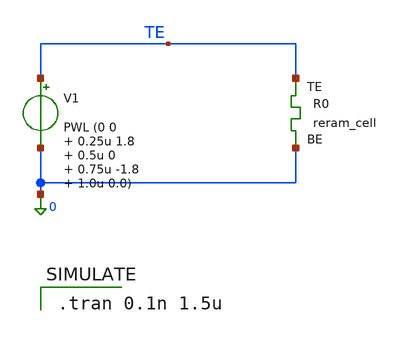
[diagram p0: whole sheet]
** sch_path: memristor_models/sky130_original/reram_example_ngspice.sch
**.subckt reram_example_ngspice
V1 TE 0 PWL (0 0 0.25u 1.8 0.5u 0 0.75u -1.8 1.0u 0.0)
XR0 TE 0 sky130_fd_pr_reram__reram_cell Tfilament_0=3.8e-9
**** begin user architecture code

.tran 0.1n 1.5u


** opencircuitdesign pdks install
.inc $::SKYWATER_MODELS/sky130_fd_pr_reram__reram_cell.spice


.control
save all
run
write reram_example_ngspice.raw
.endc



**** end user architecture code
**.ends
.end
